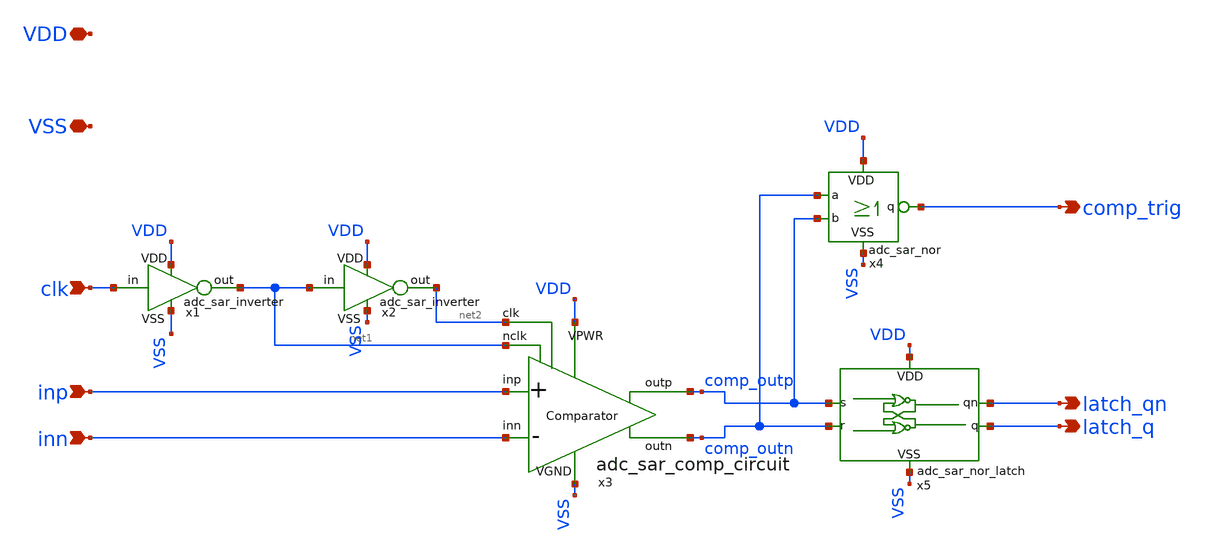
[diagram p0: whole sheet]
** sch_path: adc_sar_comp_latch.sch
**.subckt adc_sar_comp_latch VDD VSS clk inp inn comp_trig latch_qn latch_q
*.iopin VDD
*.iopin VSS
*.ipin clk
*.ipin inp
*.ipin inn
*.opin comp_trig
*.opin latch_qn
*.opin latch_q
x1 VDD VSS clk net1 adc_sar_inverter
x2 VDD VSS net1 net2 adc_sar_inverter
x3 VDD VSS net2 net1 inp inn comp_outp comp_outn adc_sar_comp_circuit
x4 comp_outp comp_outn VDD comp_trig VSS adc_sar_nor
x5 comp_outp latch_qn VDD latch_q VSS comp_outn adc_sar_nor_latch
**.ends
.end
